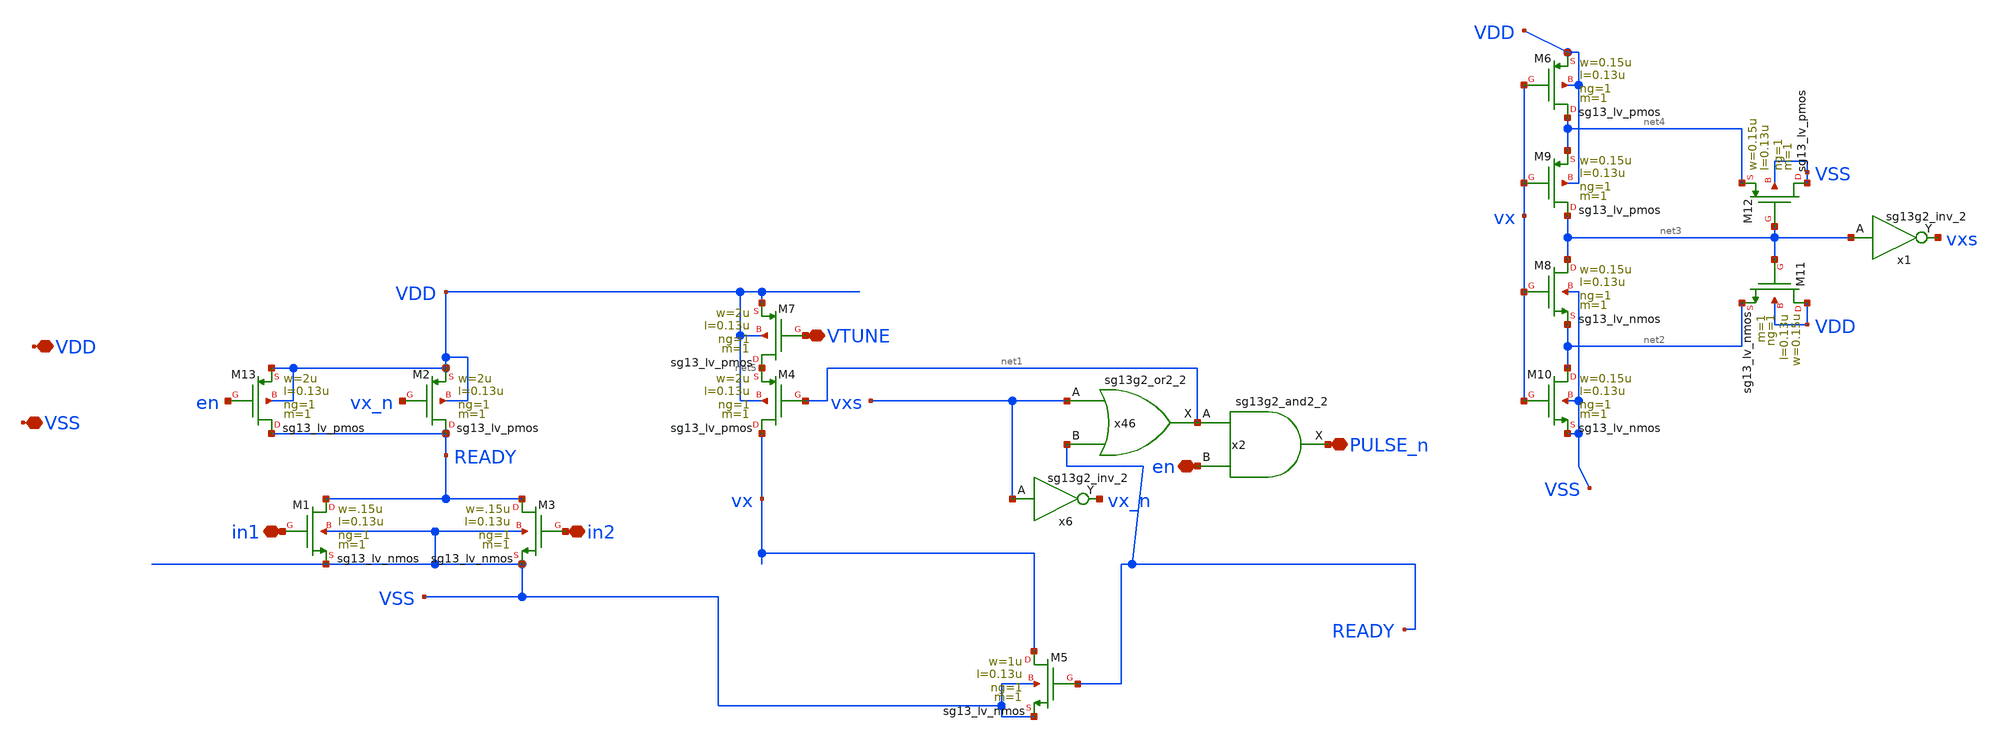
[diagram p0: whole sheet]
** sch_path: xschem/comparator/pulse_gen/pgen.sch
* IHP-GmbH/IHP-Open-PDK/ihp-sg13g2/libs.tech/xschem/sg13g2_stdcells/sg13g2_inv_2.sch:
* Copyright 2023 IHP PDK Authors
* Licensed under the Apache License, Version 2.0 (the "License");
**.subckt pgen VDD in2 in1 VSS VTUNE PULSE_n en
*.iopin VDD
*.iopin in2
*.iopin in1
*.iopin VSS
*.iopin VTUNE
*.iopin PULSE_n
*.iopin en
XM1 READY in1 VSS VSS sg13_lv_nmos w=.15u l=0.13u ng=1 m=1 mm_ok=1
XM2 READY vx_n VDD VDD sg13_lv_pmos w=2u l=0.13u ng=1 m=1 mm_ok=1
XM4 vx net1 net5 VDD sg13_lv_pmos w=2u l=0.13u ng=1 m=1 mm_ok=1
x46 net1 vxs READY VDD VSS sg13g2_or2_2
x6 vx_n vxs VDD VSS sg13g2_inv_2
XM3 READY in2 VSS VSS sg13_lv_nmos w=.15u l=0.13u ng=1 m=1 mm_ok=1
XM5 vx READY VSS VSS sg13_lv_nmos w=1u l=0.13u ng=1 m=1 mm_ok=1
XM7 net5 VTUNE VDD VDD sg13_lv_pmos w=2u l=0.13u ng=1 m=1 mm_ok=1
XM6 net4 vx VDD VDD sg13_lv_pmos w=0.15u l=0.13u ng=1 m=1 mm_ok=1
XM8 net3 vx net2 VSS sg13_lv_nmos w=0.15u l=0.13u ng=1 m=1 mm_ok=1
XM9 net3 vx net4 VDD sg13_lv_pmos w=0.15u l=0.13u ng=1 m=1 mm_ok=1
XM10 net2 vx VSS VSS sg13_lv_nmos w=0.15u l=0.13u ng=1 m=1 mm_ok=1
XM11 VDD net3 net2 VDD sg13_lv_nmos w=0.15u l=0.13u ng=1 m=1 mm_ok=1
XM12 VSS net3 net4 VSS sg13_lv_pmos w=0.15u l=0.13u ng=1 m=1 mm_ok=1
x1 vxs net3 VDD VSS sg13g2_inv_2
x2 PULSE_n net1 en VDD VSS sg13g2_and2_2
XM13 READY en VDD VDD sg13_lv_pmos w=2u l=0.13u ng=1 m=1 mm_ok=1
**.ends

* expanding   symbol:  sg13g2_stdcells/sg13g2_or2_2.sym # of pins=3
** sym_path: sg13g2_stdcells/sg13g2_or2_2.sym
** sch_path: sg13g2_stdcells/sg13g2_or2_2.sch
.subckt sg13g2_or2_2 X A B VDD VSS
*.opin X
*.ipin B
*.ipin A
*.iopin VDD
*.iopin VSS
XM1 net1 B VSS VSS sg13_lv_nmos w=550.00n l=130.00n ng=1 m=1 mm_ok=1
XM2 net1 A VSS VSS sg13_lv_nmos w=550.00n l=130.00n ng=1 m=1 mm_ok=1
XM3 X net1 VSS VSS sg13_lv_nmos w=1.48u l=130.00n ng=2 m=1 mm_ok=1
XM4 net2 A VDD VDD sg13_lv_pmos w=840.00n l=130.00n ng=1 m=1 mm_ok=1
XM5 net1 B net2 VDD sg13_lv_pmos w=840.00n l=130.00n ng=1 m=1 mm_ok=1
XM6 X net1 VDD VDD sg13_lv_pmos w=2.24u l=130.00n ng=2 m=1 mm_ok=1
.ends


* expanding   symbol:  sg13g2_stdcells/sg13g2_inv_2.sym # of pins=2
** sym_path: sg13g2_stdcells/sg13g2_inv_2.sym
** sch_path: sg13g2_stdcells/sg13g2_inv_2.sch
.subckt sg13g2_inv_2 Y A VDD VSS
*.opin Y
*.ipin A
*.iopin VDD
*.iopin VSS
XM1 Y A VSS VSS sg13_lv_nmos w=1.48u l=130.00n ng=2 m=1 mm_ok=1
XM2 Y A VDD VDD sg13_lv_pmos w=2.24u l=130.00n ng=2 m=1 mm_ok=1
.ends


* expanding   symbol:  sg13g2_stdcells/sg13g2_and2_2.sym # of pins=3
** sym_path: sg13g2_stdcells/sg13g2_and2_2.sym
** sch_path: sg13g2_stdcells/sg13g2_and2_2.sch
.subckt sg13g2_and2_2 X A B VDD VSS
*.ipin A
*.ipin B
*.opin X
*.iopin VDD
*.iopin VSS
XM1 net1 A net2 VSS sg13_lv_nmos w=640.00n l=130.00n ng=1 m=1 mm_ok=1
XM2 net2 B VSS VSS sg13_lv_nmos w=640.00n l=130.00n ng=1 m=1 mm_ok=1
XM3 X net1 VSS VSS sg13_lv_nmos w=1.48u l=130.00n ng=2 m=1 mm_ok=1
XM4 net1 B VDD VDD sg13_lv_pmos w=840.00n l=130.00n ng=1 m=1 mm_ok=1
XM5 net1 A VDD VDD sg13_lv_pmos w=840.00n l=130.00n ng=1 m=1 mm_ok=1
XM6 X net1 VDD VDD sg13_lv_pmos w=2.24u l=130.00n ng=2 m=1 mm_ok=1
.ends

.end
